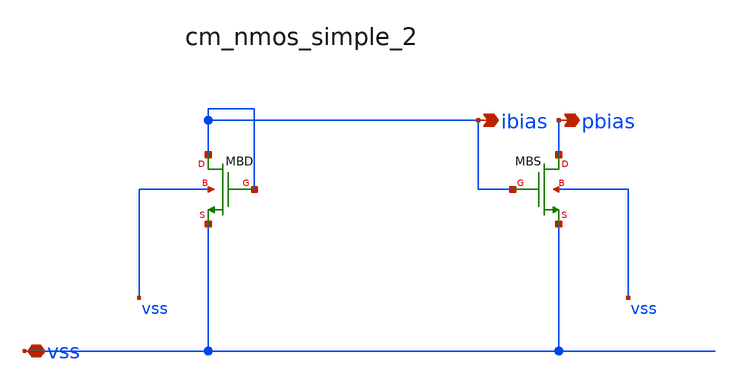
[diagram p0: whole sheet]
** sch_path: analog-db/raw/amp_022_fer_two_stage/hier/blocks/cm_nmos_simple_2.sch
**.subckt cm_nmos_simple_2 vss ibias pbias
*.iopin vss
*.opin ibias
*.opin pbias
XMBD ibias ibias vss vss sg13_lv_nmos w=x_dut_xmbd_w l=x_dut_xmbd_l ng=1 m=x_dut_xmbd_m
XMBS pbias ibias vss vss sg13_lv_nmos w=x_dut_xmbs_w l=x_dut_xmbs_l ng=1 m=x_dut_xmbs_m
**.ends
.end
